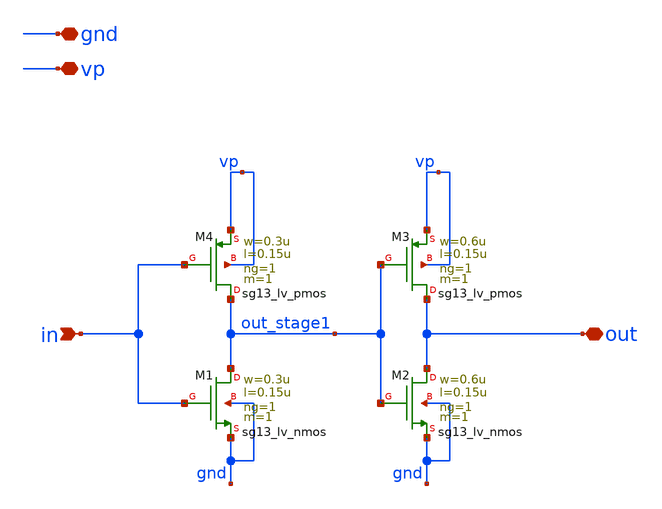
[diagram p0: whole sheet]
** sch_path: schematics/PFD/PFD_buffor.sch
**.subckt PFD_buffor gnd vp in out
*.iopin gnd
*.iopin vp
*.ipin in
*.iopin out
XM1 out_stage1 in gnd gnd sg13_lv_nmos w=0.3u l=0.15u ng=1 m=1 mm_ok=1
XM4 out_stage1 in vp vp sg13_lv_pmos w=0.3u l=0.15u ng=1 m=1 mm_ok=1
XM2 out out_stage1 gnd gnd sg13_lv_nmos w=0.6u l=0.15u ng=1 m=1 mm_ok=1
XM3 out out_stage1 vp vp sg13_lv_pmos w=0.6u l=0.15u ng=1 m=1 mm_ok=1
**.ends
.end
